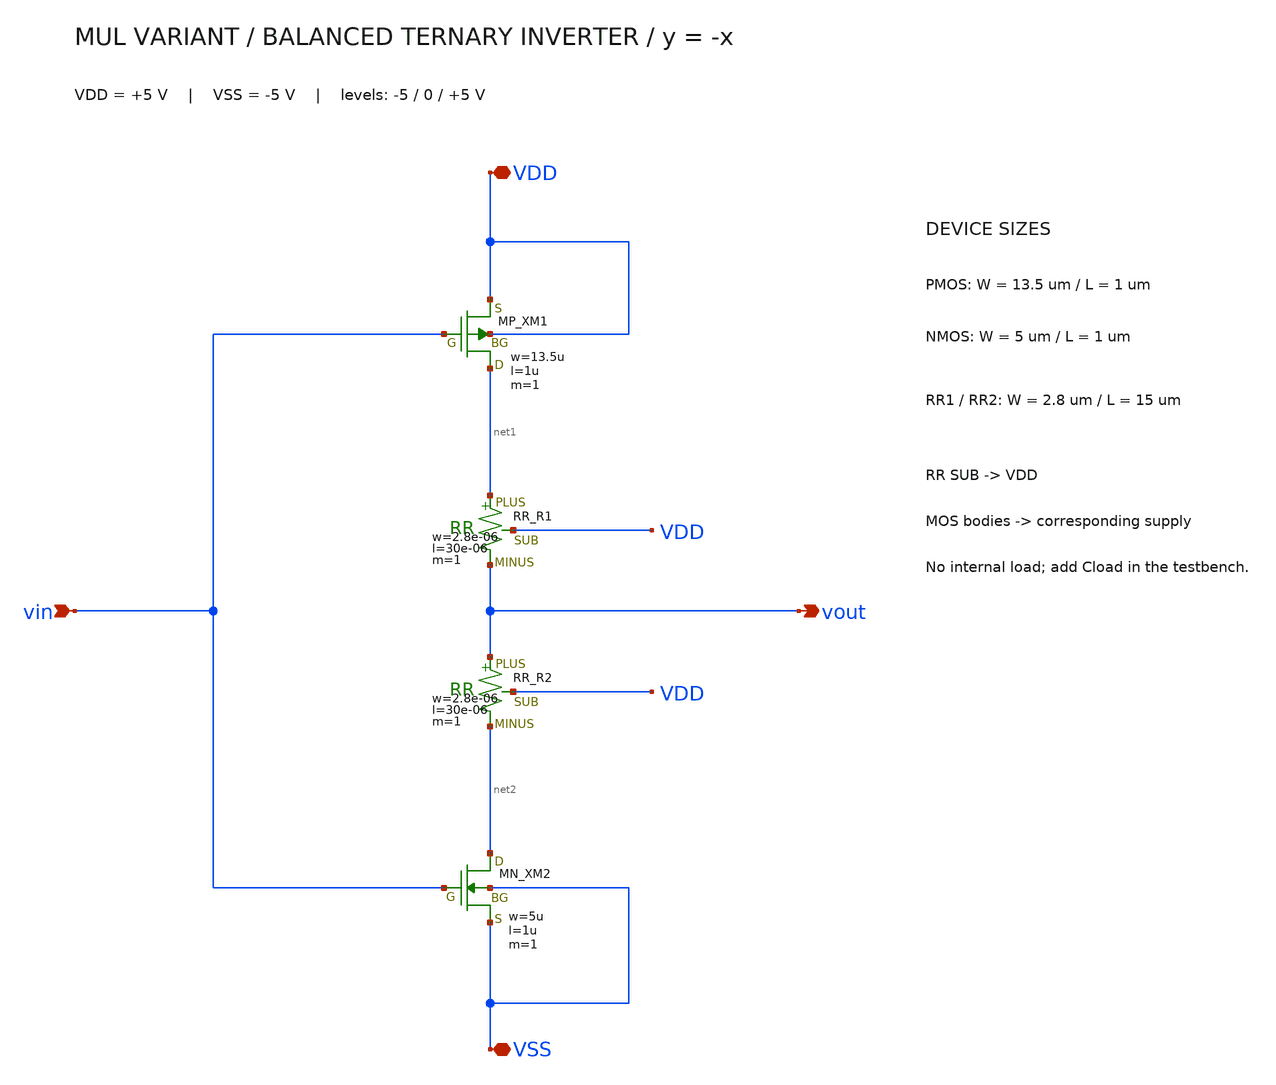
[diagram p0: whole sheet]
** sch_path: member_project/balanced-ternary-logic/PenguinEino/submission/mul_inv.sch
**.subckt mul_inv VDD vin vout VSS
*.iopin VDD
*.ipin vin
*.opin vout
*.iopin VSS
XXM1 net1 vin VDD VDD PMOS w=13.5u l=1u nrd=0 nrs=0 m=1
XR1 net1 vout VDD F_RR w=2.8e-06 l=30e-06 R=1 tc1=0 tc2=0 m=1
XR2 vout net2 VDD F_RR w=2.8e-06 l=30e-06 R=1 tc1=0 tc2=0 m=1
XXM2 net2 vin VSS VSS NMOS w=5u l=1u nrd=0 nrs=0 m=1
**.ends
.end
